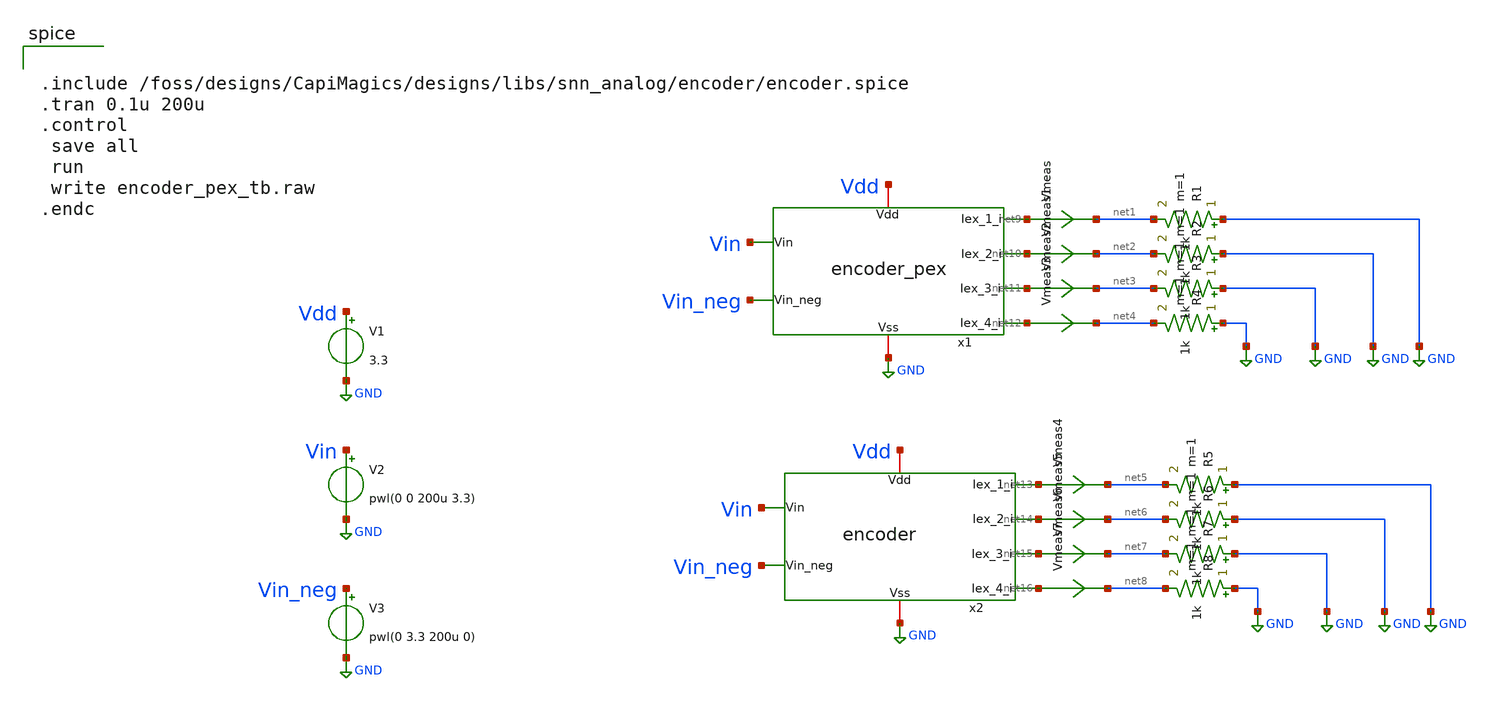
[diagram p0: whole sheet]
** sch_path: designs/libs/snn_analog/encoder/sch/encoder_pex_tb.sch
**.subckt encoder_pex_tb
R1 GND net1 1k m=1
R2 GND net2 1k m=1
R3 GND net3 1k m=1
R4 GND net4 1k m=1
Vmeas net9 net1 0
.save i(vmeas)
Vmeas1 net10 net2 0
.save i(vmeas1)
Vmeas2 net11 net3 0
.save i(vmeas2)
Vmeas3 net12 net4 0
.save i(vmeas3)
V1 Vdd GND 3.3
V2 Vin GND pwl(0 0 200u 3.3)
V3 Vin_neg GND pwl(0 3.3 200u 0)
x1 Vdd GND Vin Vin_neg net9 net10 net11 net12 encoder_pex
x2 Vdd GND Vin Vin_neg net13 net14 net15 net16 encoder
R5 GND net5 1k m=1
R6 GND net6 1k m=1
R7 GND net7 1k m=1
R8 GND net8 1k m=1
Vmeas4 net13 net5 0
.save i(vmeas4)
Vmeas5 net14 net6 0
.save i(vmeas5)
Vmeas6 net15 net7 0
.save i(vmeas6)
Vmeas7 net16 net8 0
.save i(vmeas7)
**** begin user architecture code

.include $::180MCU_MODELS/design.ngspice
.lib $::180MCU_MODELS/sm141064.ngspice typical
.lib $::180MCU_MODELS/smbb000149.ngspice typical



.include /foss/designs/CapiMagics/designs/libs/snn_analog/encoder/encoder.spice
.tran 0.1u 200u
.control
 save all
 run
 write encoder_pex_tb.raw
.endc

**** end user architecture code
**.ends

* expanding   symbol:  encoder.sym # of pins=8
** sym_path: designs/libs/snn_analog/encoder/sch/encoder.sym
** sch_path: designs/libs/snn_analog/encoder/sch/encoder.sch
.subckt encoder Vdd Vss Vin Vin_neg Iex_1_i Iex_2_i Iex_3_i Iex_4_i
*.iopin Vdd
*.iopin Vss
*.ipin Vin
*.ipin Vin_neg
*.opin Iex_1_i
*.opin Iex_4_i
*.opin Iex_2_i
*.opin Iex_3_i
XM1 x Vin a Vss nfet_03v3 L=10u W=0.5u nf=1 ad='int((nf+1)/2) * W/nf * 0.18u' as='int((nf+2)/2) * W/nf * 0.18u'
+ pd='2*int((nf+1)/2) * (W/nf + 0.18u)' ps='2*int((nf+2)/2) * (W/nf + 0.18u)' nrd='0.18u / W' nrs='0.18u / W'
+ sa=0 sb=0 sd=0 m=1
XM2 y Vin_neg a Vss nfet_03v3 L=10u W=0.5u nf=1 ad='int((nf+1)/2) * W/nf * 0.18u' as='int((nf+2)/2) * W/nf * 0.18u'
+ pd='2*int((nf+1)/2) * (W/nf + 0.18u)' ps='2*int((nf+2)/2) * (W/nf + 0.18u)' nrd='0.18u / W' nrs='0.18u / W'
+ sa=0 sb=0 sd=0 m=1
XM3 x x Vdd Vdd pfet_03v3 L=0.28u W=2u nf=1 ad='int((nf+1)/2) * W/nf * 0.18u' as='int((nf+2)/2) * W/nf * 0.18u'
+ pd='2*int((nf+1)/2) * (W/nf + 0.18u)' ps='2*int((nf+2)/2) * (W/nf + 0.18u)' nrd='0.18u / W' nrs='0.18u / W'
+ sa=0 sb=0 sd=0 m=1
XM4 y y Vdd Vdd pfet_03v3 L=0.28u W=2u nf=1 ad='int((nf+1)/2) * W/nf * 0.18u' as='int((nf+2)/2) * W/nf * 0.18u'
+ pd='2*int((nf+1)/2) * (W/nf + 0.18u)' ps='2*int((nf+2)/2) * (W/nf + 0.18u)' nrd='0.18u / W' nrs='0.18u / W'
+ sa=0 sb=0 sd=0 m=1
XM5 Iex_2_i x Vdd Vdd pfet_03v3 L=1.86u W=0.93u nf=1 ad='int((nf+1)/2) * W/nf * 0.18u' as='int((nf+2)/2) * W/nf * 0.18u'
+ pd='2*int((nf+1)/2) * (W/nf + 0.18u)' ps='2*int((nf+2)/2) * (W/nf + 0.18u)' nrd='0.18u / W' nrs='0.18u / W'
+ sa=0 sb=0 sd=0 m=1
XM7 Iex_3_i y Vdd Vdd pfet_03v3 L=1.86u W=0.93u nf=1 ad='int((nf+1)/2) * W/nf * 0.18u' as='int((nf+2)/2) * W/nf * 0.18u'
+ pd='2*int((nf+1)/2) * (W/nf + 0.18u)' ps='2*int((nf+2)/2) * (W/nf + 0.18u)' nrd='0.18u / W' nrs='0.18u / W'
+ sa=0 sb=0 sd=0 m=1
XM9 a net1 Vss Vss nfet_03v3 L=0.28u W=0.5u nf=1 ad='int((nf+1)/2) * W/nf * 0.18u' as='int((nf+2)/2) * W/nf * 0.18u'
+ pd='2*int((nf+1)/2) * (W/nf + 0.18u)' ps='2*int((nf+2)/2) * (W/nf + 0.18u)' nrd='0.18u / W' nrs='0.18u / W'
+ sa=0 sb=0 sd=0 m=1
XM10 net1 net1 Vss Vss nfet_03v3 L=0.28u W=0.5u nf=1 ad='int((nf+1)/2) * W/nf * 0.18u' as='int((nf+2)/2) * W/nf * 0.18u'
+ pd='2*int((nf+1)/2) * (W/nf + 0.18u)' ps='2*int((nf+2)/2) * (W/nf + 0.18u)' nrd='0.18u / W' nrs='0.18u / W'
+ sa=0 sb=0 sd=0 m=1
XM11 net1 net1 Vdd Vdd pfet_03v3 L=0.28u W=0.5u nf=1 ad='int((nf+1)/2) * W/nf * 0.18u' as='int((nf+2)/2) * W/nf * 0.18u'
+ pd='2*int((nf+1)/2) * (W/nf + 0.18u)' ps='2*int((nf+2)/2) * (W/nf + 0.18u)' nrd='0.18u / W' nrs='0.18u / W'
+ sa=0 sb=0 sd=0 m=1
XM6 Iex_4_i y Vdd Vdd pfet_03v3 L=1.86u W=0.93u nf=1 ad='int((nf+1)/2) * W/nf * 0.18u' as='int((nf+2)/2) * W/nf * 0.18u'
+ pd='2*int((nf+1)/2) * (W/nf + 0.18u)' ps='2*int((nf+2)/2) * (W/nf + 0.18u)' nrd='0.18u / W' nrs='0.18u / W'
+ sa=0 sb=0 sd=0 m=1
XM8 Iex_1_i x Vdd Vdd pfet_03v3 L=1.86u W=0.93u nf=1 ad='int((nf+1)/2) * W/nf * 0.18u' as='int((nf+2)/2) * W/nf * 0.18u'
+ pd='2*int((nf+1)/2) * (W/nf + 0.18u)' ps='2*int((nf+2)/2) * (W/nf + 0.18u)' nrd='0.18u / W' nrs='0.18u / W'
+ sa=0 sb=0 sd=0 m=1
.ends

.GLOBAL GND
.end
